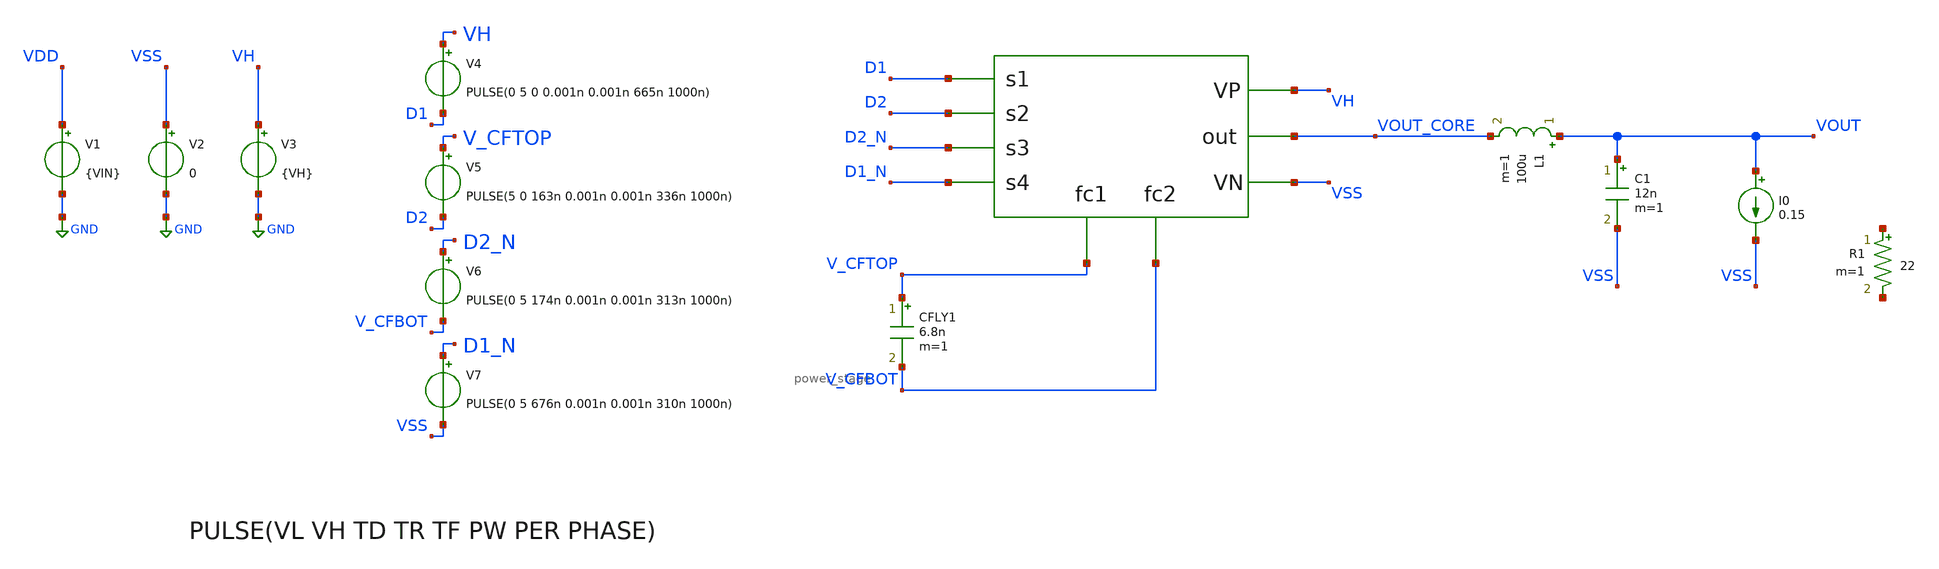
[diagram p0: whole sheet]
** sch_path: xschem/hierarchy_sch/DCDC_5V_FINAL/DCDC_v1p5_1MHz_NMOS_PMOS_sng.sch
**.subckt DCDC_v1p5_1MHz_NMOS_PMOS_sng
V1 VDD GND {VIN}
V4 VH D1 PULSE(0 5 0 0.001n 0.001n 665n 1000n)
V2 VSS GND 0
V6 D2_N V_CFBOT PULSE(0 5 174n 0.001n 0.001n 313n 1000n)
V3 VH GND {VH}
V5 V_CFTOP D2 PULSE(5 0 163n 0.001n 0.001n 336n 1000n)
V7 D1_N VSS PULSE(0 5 676n 0.001n 0.001n 310n 1000n)
X1 D1 D2 D2_N D1_N V_CFTOP V_CFBOT VOUT_CORE VH VSS power_stage
CFLY1 V_CFTOP V_CFBOT 6.8n m=1
L1 VOUT VOUT_CORE 100u m=1
C1 VOUT VSS 12n m=1
I0 VOUT VSS 0.15
R1 net1 net2 22 m=1
**** begin user architecture code


.param VIN = 5
.param VH = 5
.param RL = 50
.option scale=1e-6
*.option temp=70
.ic v(V_CFTOP) = VH/2
.ic v(vout)=0
.ic v(V_CFBOT) = 0
*.probe vd(MP2:G:S)
*.save all
*.save v(d1) v(d2) v(d1top_5v) v(d2_5v) v(d2bot_5v) v(d1bot_5v) v(vout) v(vout_core) v(vdd) v(vh) i(v1) i(v5) i(vmeas) v(v_cftop,v_cfbot)
.save v(D1) v(D2) v(D1_N) v(D2_N) v(VOUT) v(VOUT_CORE) v(vdd) v(vh) i(v1) i(v3) i(vmeas) v(v_cftop,v_cfbot) v(D1,v_cftop) v(D2,vout_core) v(D2_N,v_cfbot) v(D1_Nv,VSS)
.param mc_mm_switch=0
*.lib /home/jorge/Documents/Postdoc/share/pdk/sky130A/libs.tech/ngspice/sky130.lib.spice tt
*.lib /usr/share/pdk/sky130A/libs.tech/ngspice/sky130.lib.spice ss
.lib /foss/pdk/sky130A/libs.tech/ngspice/sky130.lib.spice TT
*.include /usr/share/pdk/sky130A/libs.ref/sky130_fd_sc_hvl/spice/sky130_fd_sc_hvl.spice
*.include /home/jorge/Documents/Postdoc/share/pdk/sky130A/libs.ref/sky130_fd_sc_hvl/spice/sky130_fd_sc_hvl.spice
.options savecurrents
.control
*save all
tran 100n 3u
write DCDC_v1p4_5MHz_NMOS_PMOS.raw
*wrdata
*+ ~/Documents/Postdoc/chipathon2022/3LFCC_AC3E/xschem/dev_switches/DCDC_5V_FINAL/3LFCC_v1p4.txt tran.v(vout) tran.i(vmeas) tran.v(vdd) tran.i(v1) tran.v(vh) tran.i(v5)
wrdata /foss/designs/personal/3LFCC_AC3E/xschem/dev_switches/DCDC_5V_FINAL/3LFCC_v1p4.txt
+ tran.v(vout) tran.i(v3) tran.i(v1)

*plot v(d1top_5v) v(d2_5v)
*plot v(d2bot_5v) v(d1bot_5v)
plot v(v_cftop,v_cfbot) v(vout)
plot v(D1,VH) v(D1_N,VSS)
plot v(D2,V_CFTOP) v(D2_N,V_CFBOT)
plot v(vout) v(vout_core)



*plot v(d1top_5v) v(d2_5v) v(d2bot_5v) v(d1bot_5v) v(v_cftop,v_cfbot) v(vout)
*plot v(v_cftop,v_cfbot) v(vout)
.endc


**** end user architecture code
**.ends

* expanding   symbol:  personal/3LFCC_AC3E/xschem/hierarchy_sch/power_stage.sym # of pins=9
** sym_path: xschem/hierarchy_sch/power_stage.sym
** sch_path: xschem/hierarchy_sch/power_stage.sch
.subckt power_stage s1 s2 s3 s4 fc1 fc2 out VP VN
*.ipin s1
*.ipin s2
*.ipin s3
*.ipin s4
*.iopin VP
*.iopin VN
*.opin out
*.opin fc1
*.opin fc2
X1 s2 fc1 s1 VP out transistor_group_one
X2 s4 fc2 s3 out VN transistor_group_two
.ends


* expanding   symbol:  personal/3LFCC_AC3E/xschem/hierarchy_sch/transistor_group_one.sym # of pins=5
** sym_path: xschem/hierarchy_sch/transistor_group_one.sym
** sch_path: xschem/hierarchy_sch/transistor_group_one.sch
.subckt transistor_group_one s2 fc1 s1 VP out
*.iopin VP
*.ipin s1
*.ipin s2
*.opin fc1
*.iopin out
XM3 out s2 fc1 fc1 sky130_fd_pr__pfet_g5v0d10v5 L=0.5 W=4.38 nf=1 ad='int((nf+1)/2) * W/nf * 0.29' as='int((nf+2)/2) * W/nf * 0.29'
+ pd='2*int((nf+1)/2) * (W/nf + 0.29)' ps='2*int((nf+2)/2) * (W/nf + 0.29)' nrd='0.29 / W' nrs='0.29 / W'
+ sa=0 sb=0 sd=0 mult=4506 m=4506
XM4 fc1 s1 VP VP sky130_fd_pr__pfet_g5v0d10v5 L=0.5 W=4.38 nf=1 ad='int((nf+1)/2) * W/nf * 0.29' as='int((nf+2)/2) * W/nf * 0.29'
+ pd='2*int((nf+1)/2) * (W/nf + 0.29)' ps='2*int((nf+2)/2) * (W/nf + 0.29)' nrd='0.29 / W' nrs='0.29 / W'
+ sa=0 sb=0 sd=0 mult=4506 m=4506
.ends


* expanding   symbol:  personal/3LFCC_AC3E/xschem/hierarchy_sch/transistor_group_two.sym # of pins=5
** sym_path: xschem/hierarchy_sch/transistor_group_two.sym
** sch_path: xschem/hierarchy_sch/transistor_group_two.sch
.subckt transistor_group_two s4 fc2 s3 out VN
*.iopin out
*.ipin s3
*.ipin s4
*.opin fc2
*.iopin VN
XM1 out s3 fc2 fc2 sky130_fd_pr__nfet_g5v0d10v5 L=0.5 W=4.38 nf=1 ad='int((nf+1)/2) * W/nf * 0.29' as='int((nf+2)/2) * W/nf * 0.29'
+ pd='2*int((nf+1)/2) * (W/nf + 0.29)' ps='2*int((nf+2)/2) * (W/nf + 0.29)' nrd='0.29 / W' nrs='0.29 / W'
+ sa=0 sb=0 sd=0 mult=2520 m=2520
XM2 fc2 s4 VN VN sky130_fd_pr__nfet_g5v0d10v5 L=0.5 W=4.38 nf=1 ad='int((nf+1)/2) * W/nf * 0.29' as='int((nf+2)/2) * W/nf * 0.29'
+ pd='2*int((nf+1)/2) * (W/nf + 0.29)' ps='2*int((nf+2)/2) * (W/nf + 0.29)' nrd='0.29 / W' nrs='0.29 / W'
+ sa=0 sb=0 sd=0 mult=2520 m=2520
.ends

.GLOBAL GND
.end
